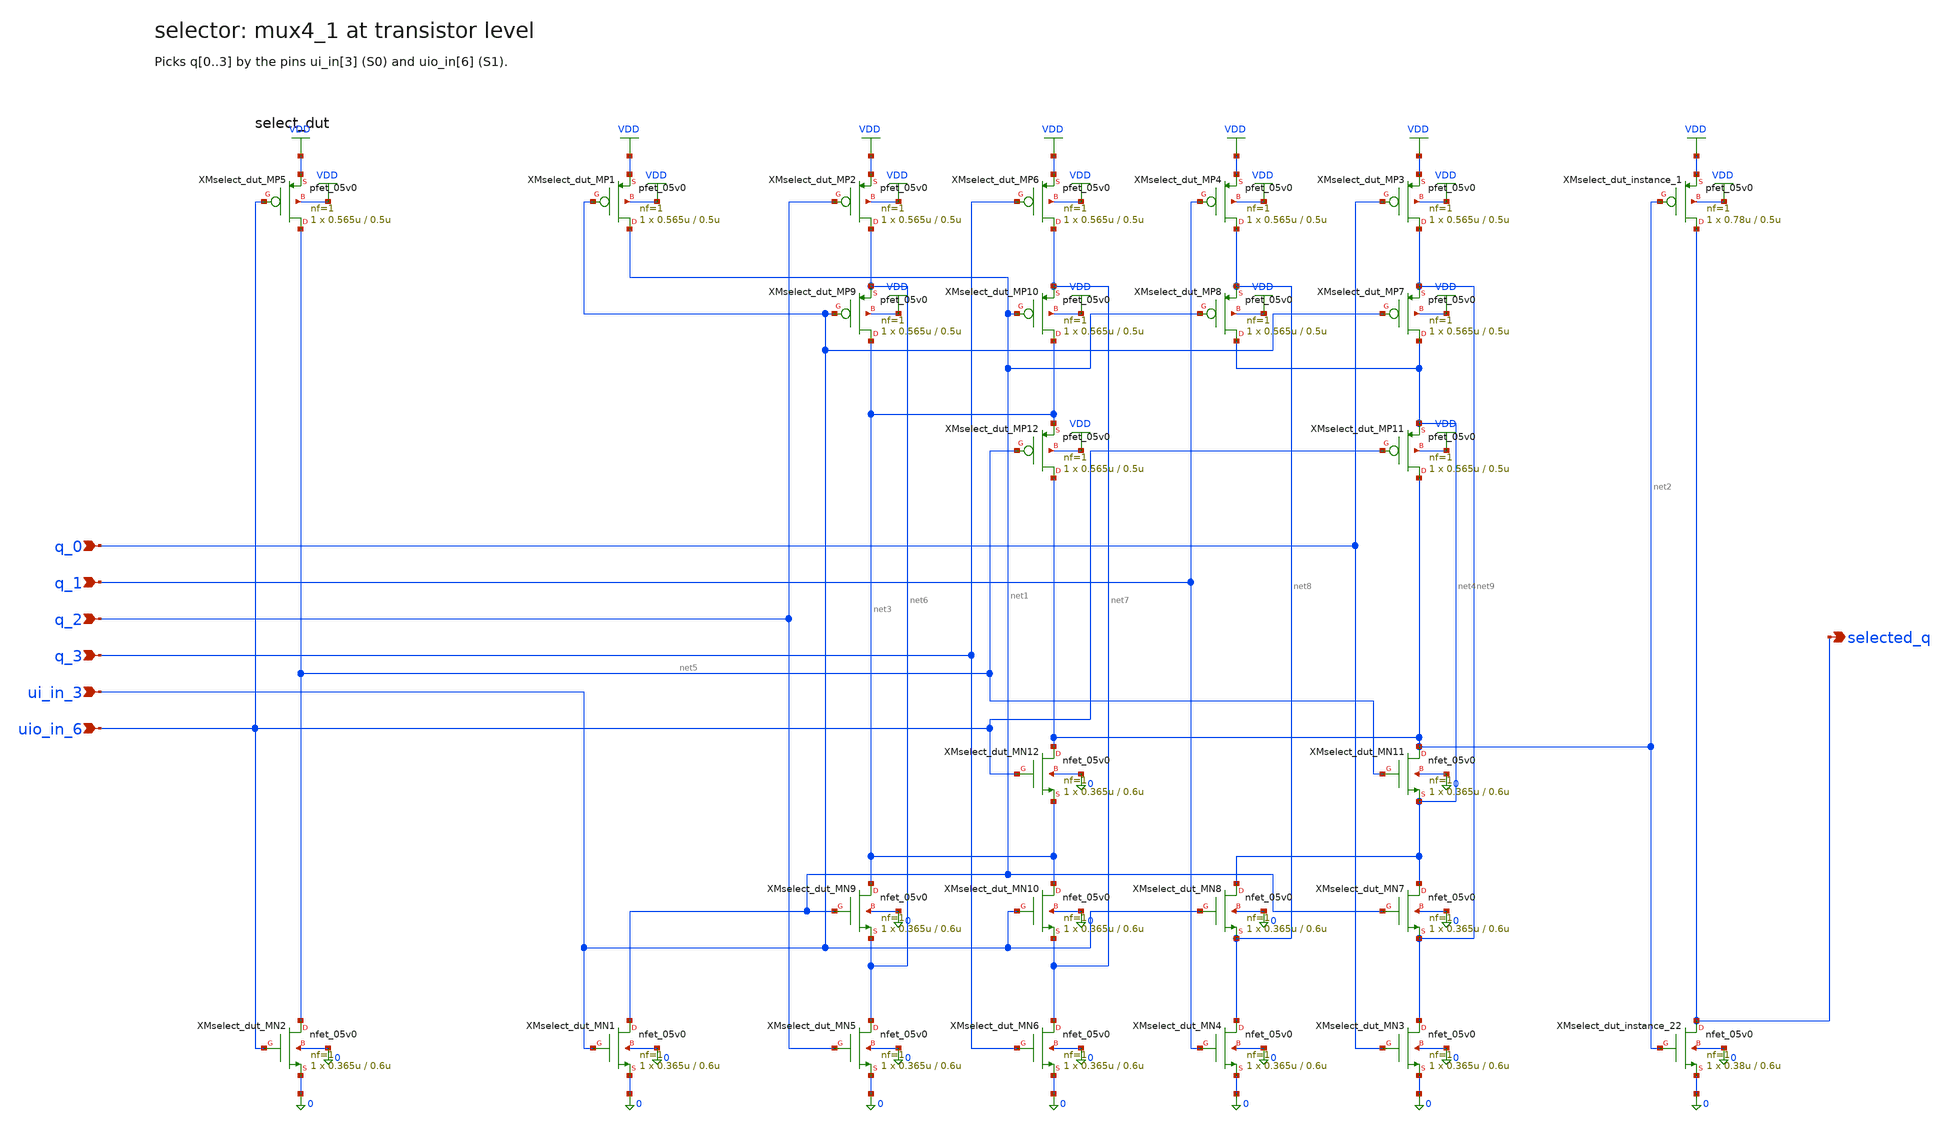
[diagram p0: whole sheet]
** sch_path: xschem/flat/selector.sch
**.subckt selector q_0 q_1 q_2 q_3 ui_in_3 uio_in_6 selected_q
*.ipin q_0
*.ipin q_1
*.ipin q_2
*.ipin q_3
*.ipin ui_in_3
*.ipin uio_in_6
*.opin selected_q
XMselect_dut_MN5 net6 q_2 0 0 nfet_05v0 L=0.6u W=0.365u nf=1 ad=1.825e-13 as=1.825e-13 pd=1.73e-06
+ ps=1.73e-06 nrd=0 nrs=0 sa=0 sb=0 sd=0 m=1
XMselect_dut_MN9 net3 net1 net6 0 nfet_05v0 L=0.6u W=0.365u nf=1 ad=1.825e-13 as=1.825e-13
+ pd=1.73e-06 ps=1.73e-06 nrd=0 nrs=0 sa=0 sb=0 sd=0 m=1
XMselect_dut_MN10 net3 ui_in_3 net7 0 nfet_05v0 L=0.6u W=0.365u nf=1 ad=1.825e-13 as=1.825e-13
+ pd=1.73e-06 ps=1.73e-06 nrd=0 nrs=0 sa=0 sb=0 sd=0 m=1
XMselect_dut_MN6 net7 q_3 0 0 nfet_05v0 L=0.6u W=0.365u nf=1 ad=1.825e-13 as=1.825e-13 pd=1.73e-06
+ ps=1.73e-06 nrd=0 nrs=0 sa=0 sb=0 sd=0 m=1
XMselect_dut_instance_22 selected_q net2 0 0 nfet_05v0 L=0.6u W=0.38u nf=1 ad=1.9e-13 as=1.9e-13
+ pd=1.76e-06 ps=1.76e-06 nrd=0 nrs=0 sa=0 sb=0 sd=0 m=1
XMselect_dut_MN12 net2 uio_in_6 net3 0 nfet_05v0 L=0.6u W=0.365u nf=1 ad=1.825e-13 as=1.825e-13
+ pd=1.73e-06 ps=1.73e-06 nrd=0 nrs=0 sa=0 sb=0 sd=0 m=1
XMselect_dut_MN11 net2 net5 net4 0 nfet_05v0 L=0.6u W=0.365u nf=1 ad=1.825e-13 as=1.825e-13
+ pd=1.73e-06 ps=1.73e-06 nrd=0 nrs=0 sa=0 sb=0 sd=0 m=1
XMselect_dut_MN2 net5 uio_in_6 0 0 nfet_05v0 L=0.6u W=0.365u nf=1 ad=1.825e-13 as=1.825e-13
+ pd=1.73e-06 ps=1.73e-06 nrd=0 nrs=0 sa=0 sb=0 sd=0 m=1
XMselect_dut_MN4 net8 q_1 0 0 nfet_05v0 L=0.6u W=0.365u nf=1 ad=1.825e-13 as=1.825e-13 pd=1.73e-06
+ ps=1.73e-06 nrd=0 nrs=0 sa=0 sb=0 sd=0 m=1
XMselect_dut_MN8 net4 ui_in_3 net8 0 nfet_05v0 L=0.6u W=0.365u nf=1 ad=1.825e-13 as=1.825e-13
+ pd=1.73e-06 ps=1.73e-06 nrd=0 nrs=0 sa=0 sb=0 sd=0 m=1
XMselect_dut_MN7 net4 net1 net9 0 nfet_05v0 L=0.6u W=0.365u nf=1 ad=1.825e-13 as=1.825e-13
+ pd=1.73e-06 ps=1.73e-06 nrd=0 nrs=0 sa=0 sb=0 sd=0 m=1
XMselect_dut_MN3 net9 q_0 0 0 nfet_05v0 L=0.6u W=0.365u nf=1 ad=1.825e-13 as=1.825e-13 pd=1.73e-06
+ ps=1.73e-06 nrd=0 nrs=0 sa=0 sb=0 sd=0 m=1
XMselect_dut_MN1 net1 ui_in_3 0 0 nfet_05v0 L=0.6u W=0.365u nf=1 ad=1.825e-13 as=1.825e-13
+ pd=1.73e-06 ps=1.73e-06 nrd=0 nrs=0 sa=0 sb=0 sd=0 m=1
XMselect_dut_MP2 net6 q_2 VDD VDD pfet_05v0 L=0.5u W=0.565u nf=1 ad=2.825e-13 as=2.825e-13
+ pd=2.13e-06 ps=2.13e-06 nrd=0 nrs=0 sa=0 sb=0 sd=0 m=1
XMselect_dut_MP9 net3 ui_in_3 net6 VDD pfet_05v0 L=0.5u W=0.565u nf=1 ad=2.825e-13 as=2.825e-13
+ pd=2.13e-06 ps=2.13e-06 nrd=0 nrs=0 sa=0 sb=0 sd=0 m=1
XMselect_dut_MP10 net3 net1 net7 VDD pfet_05v0 L=0.5u W=0.565u nf=1 ad=2.825e-13 as=2.825e-13
+ pd=2.13e-06 ps=2.13e-06 nrd=0 nrs=0 sa=0 sb=0 sd=0 m=1
XMselect_dut_MP6 net7 q_3 VDD VDD pfet_05v0 L=0.5u W=0.565u nf=1 ad=2.825e-13 as=2.825e-13
+ pd=2.13e-06 ps=2.13e-06 nrd=0 nrs=0 sa=0 sb=0 sd=0 m=1
XMselect_dut_instance_1 selected_q net2 VDD VDD pfet_05v0 L=0.5u W=0.78u nf=1 ad=3.9e-13 as=3.9e-13
+ pd=2.56e-06 ps=2.56e-06 nrd=0 nrs=0 sa=0 sb=0 sd=0 m=1
XMselect_dut_MP12 net2 net5 net3 VDD pfet_05v0 L=0.5u W=0.565u nf=1 ad=2.825e-13 as=2.825e-13
+ pd=2.13e-06 ps=2.13e-06 nrd=0 nrs=0 sa=0 sb=0 sd=0 m=1
XMselect_dut_MP11 net2 uio_in_6 net4 VDD pfet_05v0 L=0.5u W=0.565u nf=1 ad=2.825e-13 as=2.825e-13
+ pd=2.13e-06 ps=2.13e-06 nrd=0 nrs=0 sa=0 sb=0 sd=0 m=1
XMselect_dut_MP5 net5 uio_in_6 VDD VDD pfet_05v0 L=0.5u W=0.565u nf=1 ad=2.825e-13 as=2.825e-13
+ pd=2.13e-06 ps=2.13e-06 nrd=0 nrs=0 sa=0 sb=0 sd=0 m=1
XMselect_dut_MP4 net8 q_1 VDD VDD pfet_05v0 L=0.5u W=0.565u nf=1 ad=2.825e-13 as=2.825e-13
+ pd=2.13e-06 ps=2.13e-06 nrd=0 nrs=0 sa=0 sb=0 sd=0 m=1
XMselect_dut_MP8 net4 net1 net8 VDD pfet_05v0 L=0.5u W=0.565u nf=1 ad=2.825e-13 as=2.825e-13
+ pd=2.13e-06 ps=2.13e-06 nrd=0 nrs=0 sa=0 sb=0 sd=0 m=1
XMselect_dut_MP7 net4 ui_in_3 net9 VDD pfet_05v0 L=0.5u W=0.565u nf=1 ad=2.825e-13 as=2.825e-13
+ pd=2.13e-06 ps=2.13e-06 nrd=0 nrs=0 sa=0 sb=0 sd=0 m=1
XMselect_dut_MP3 net9 q_0 VDD VDD pfet_05v0 L=0.5u W=0.565u nf=1 ad=2.825e-13 as=2.825e-13
+ pd=2.13e-06 ps=2.13e-06 nrd=0 nrs=0 sa=0 sb=0 sd=0 m=1
XMselect_dut_MP1 net1 ui_in_3 VDD VDD pfet_05v0 L=0.5u W=0.565u nf=1 ad=2.825e-13 as=2.825e-13
+ pd=2.13e-06 ps=2.13e-06 nrd=0 nrs=0 sa=0 sb=0 sd=0 m=1
**.ends
.GLOBAL VDD
.end
